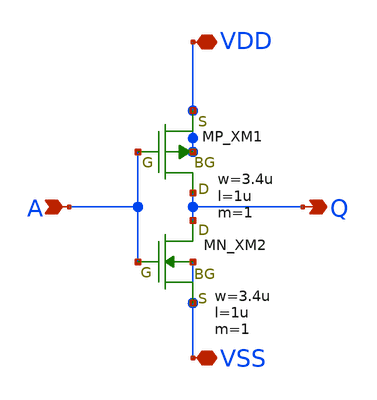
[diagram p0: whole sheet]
** sch_path: schematic/20250924_OSS_Workshop/Qdai/inverter_MUX_01/inv_kanaya.sch
**.subckt inv_kanaya A VDD VSS Q
*.ipin A
*.iopin VDD
*.iopin VSS
*.opin Q
XM1 Q A VDD VDD PMOS w=3.4u l=1u as=0 ad=0 ps=0 pd=0 nrd=0 nrs=0 m=1
XM2 Q A VSS VSS NMOS w=3.4u l=1u as=0 ad=0 ps=0 pd=0 nrd=0 nrs=0 m=1
**.ends
.end
